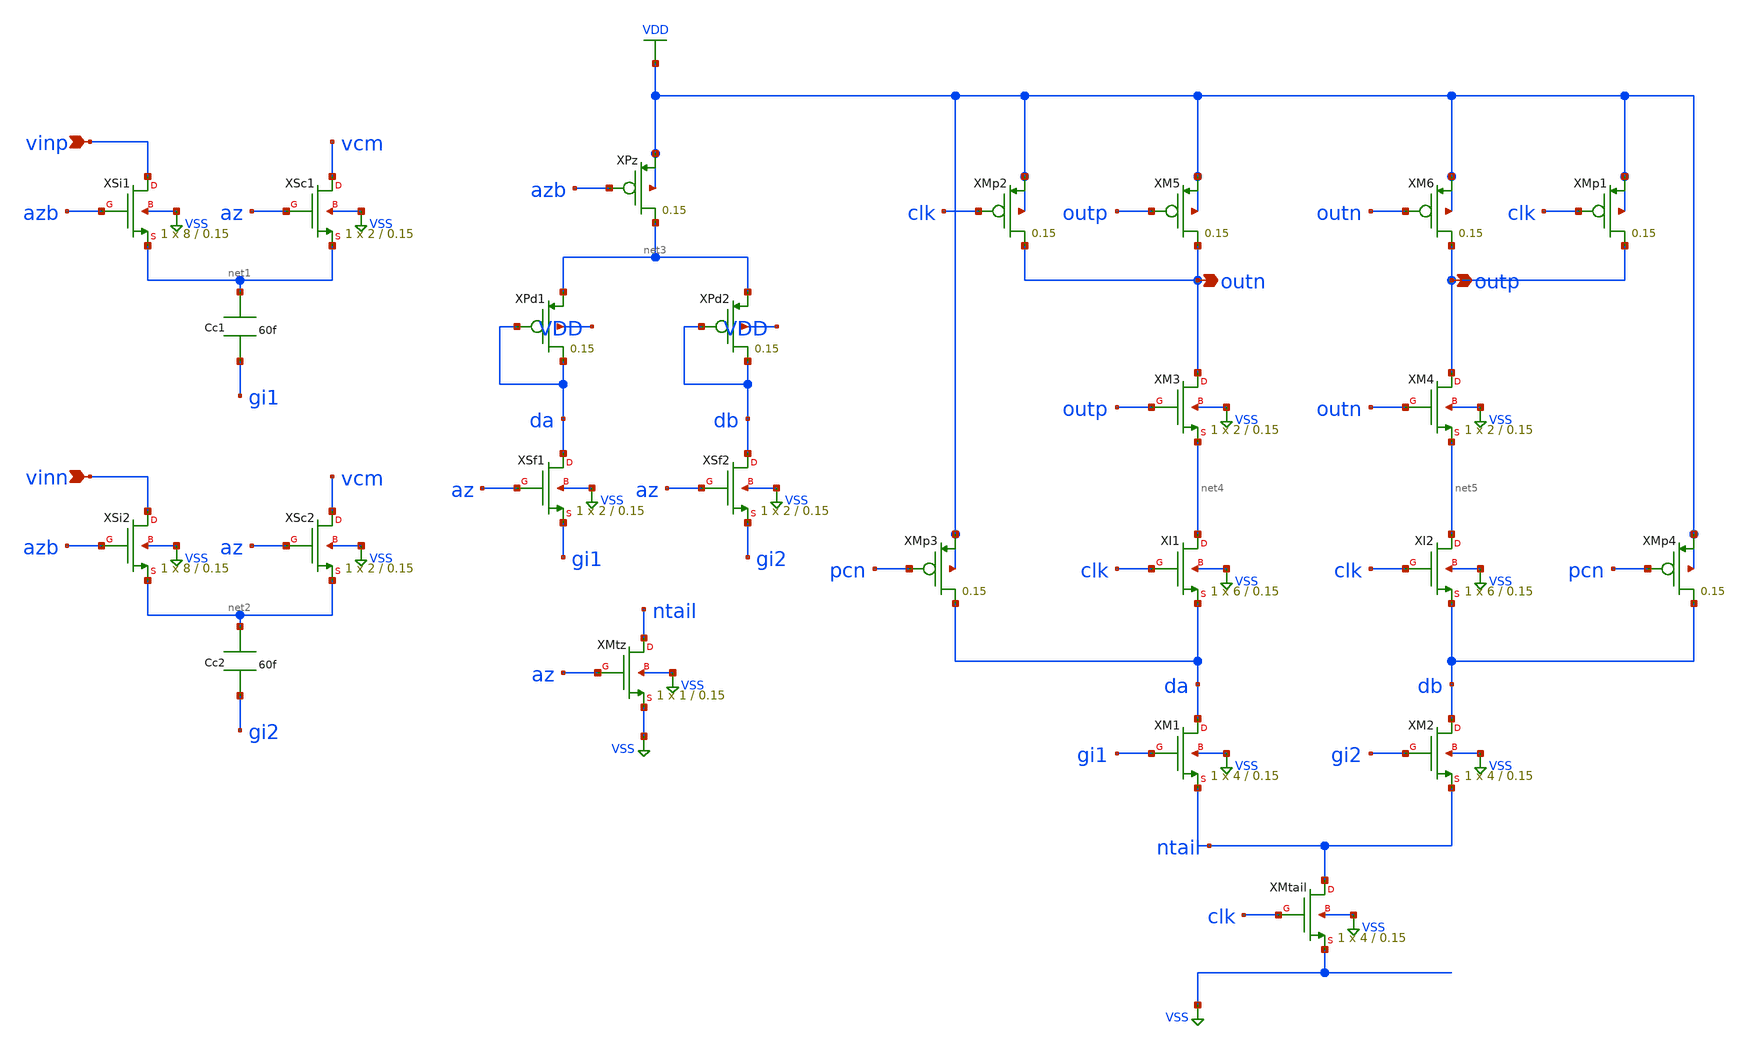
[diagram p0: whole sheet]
** sch_path: eda/hero/schematics/dong_autozero.sch
**.subckt dong_autozero vinp vinn outn outp
*.ipin vinp
*.ipin vinn
*.opin outn
*.opin outp
XXSi1 vinp azb net1 VSS sky130_fd_pr__sky130_fd_pr__nfet_01v8 L=0.15 W=8 nrd='0.29 / W' nrs='0.29 / W'
+ sa=0 sb=0 sd=0 mult=1 m=1
XXSc1 vcm az net1 VSS sky130_fd_pr__sky130_fd_pr__nfet_01v8 L=0.15 W=2 nrd='0.29 / W' nrs='0.29 / W'
+ sa=0 sb=0 sd=0 mult=1 m=1
XXSi2 vinn azb net2 VSS sky130_fd_pr__sky130_fd_pr__nfet_01v8 L=0.15 W=8 nrd='0.29 / W' nrs='0.29 / W'
+ sa=0 sb=0 sd=0 mult=1 m=1
XXSc2 vcm az net2 VSS sky130_fd_pr__sky130_fd_pr__nfet_01v8 L=0.15 W=2 nrd='0.29 / W' nrs='0.29 / W'
+ sa=0 sb=0 sd=0 mult=1 m=1
XXPz net3 azb VDD VDD sky130_fd_pr__sky130_fd_pr__pfet_01v8 L=0.15 W=4 nrd='0.29 / W' nrs='0.29 / W'
+ sa=0 sb=0 sd=0 mult=1 m=1
XXPd1 da da net3 VDD sky130_fd_pr__sky130_fd_pr__pfet_01v8 L=0.15 W=3 nrd='0.29 / W' nrs='0.29 / W' sa=0
+ sb=0 sd=0 mult=1 m=1
XXPd2 db db net3 VDD sky130_fd_pr__sky130_fd_pr__pfet_01v8 L=0.15 W=3 nrd='0.29 / W' nrs='0.29 / W' sa=0
+ sb=0 sd=0 mult=1 m=1
XXSf1 da az gi1 VSS sky130_fd_pr__sky130_fd_pr__nfet_01v8 L=0.15 W=2 nrd='0.29 / W' nrs='0.29 / W' sa=0
+ sb=0 sd=0 mult=1 m=1
XXSf2 db az gi2 VSS sky130_fd_pr__sky130_fd_pr__nfet_01v8 L=0.15 W=2 nrd='0.29 / W' nrs='0.29 / W' sa=0
+ sb=0 sd=0 mult=1 m=1
XXMtz ntail az VSS VSS sky130_fd_pr__sky130_fd_pr__nfet_01v8 L=0.15 W=1 nrd='0.29 / W' nrs='0.29 / W'
+ sa=0 sb=0 sd=0 mult=1 m=1
XXMp2 outn clk VDD VDD sky130_fd_pr__sky130_fd_pr__pfet_01v8 L=0.15 W=2 nrd='0.29 / W' nrs='0.29 / W'
+ sa=0 sb=0 sd=0 mult=1 m=1
XXM5 outn outp VDD VDD sky130_fd_pr__sky130_fd_pr__pfet_01v8 L=0.15 W=2 nrd='0.29 / W' nrs='0.29 / W'
+ sa=0 sb=0 sd=0 mult=1 m=1
XXM6 outp outn VDD VDD sky130_fd_pr__sky130_fd_pr__pfet_01v8 L=0.15 W=2 nrd='0.29 / W' nrs='0.29 / W'
+ sa=0 sb=0 sd=0 mult=1 m=1
XXMp1 outp clk VDD VDD sky130_fd_pr__sky130_fd_pr__pfet_01v8 L=0.15 W=2 nrd='0.29 / W' nrs='0.29 / W'
+ sa=0 sb=0 sd=0 mult=1 m=1
XXM3 outn outp net4 VSS sky130_fd_pr__sky130_fd_pr__nfet_01v8 L=0.15 W=2 nrd='0.29 / W' nrs='0.29 / W'
+ sa=0 sb=0 sd=0 mult=1 m=1
XXM4 outp outn net5 VSS sky130_fd_pr__sky130_fd_pr__nfet_01v8 L=0.15 W=2 nrd='0.29 / W' nrs='0.29 / W'
+ sa=0 sb=0 sd=0 mult=1 m=1
XXMp3 da pcn VDD VDD sky130_fd_pr__sky130_fd_pr__pfet_01v8 L=0.15 W=2 nrd='0.29 / W' nrs='0.29 / W' sa=0
+ sb=0 sd=0 mult=1 m=1
XXI1 net4 clk da VSS sky130_fd_pr__sky130_fd_pr__nfet_01v8 L=0.15 W=6 nrd='0.29 / W' nrs='0.29 / W' sa=0
+ sb=0 sd=0 mult=1 m=1
XXI2 net5 clk db VSS sky130_fd_pr__sky130_fd_pr__nfet_01v8 L=0.15 W=6 nrd='0.29 / W' nrs='0.29 / W' sa=0
+ sb=0 sd=0 mult=1 m=1
XXMp4 db pcn VDD VDD sky130_fd_pr__sky130_fd_pr__pfet_01v8 L=0.15 W=2 nrd='0.29 / W' nrs='0.29 / W' sa=0
+ sb=0 sd=0 mult=1 m=1
XXM1 da gi1 ntail VSS sky130_fd_pr__sky130_fd_pr__nfet_01v8 L=0.15 W=4 nrd='0.29 / W' nrs='0.29 / W'
+ sa=0 sb=0 sd=0 mult=1 m=1
XXM2 db gi2 ntail VSS sky130_fd_pr__sky130_fd_pr__nfet_01v8 L=0.15 W=4 nrd='0.29 / W' nrs='0.29 / W'
+ sa=0 sb=0 sd=0 mult=1 m=1
XXMtail ntail clk VSS VSS sky130_fd_pr__sky130_fd_pr__nfet_01v8 L=0.15 W=4 nrd='0.29 / W' nrs='0.29 / W'
+ sa=0 sb=0 sd=0 mult=1 m=1
Cc1 net1 gi1 60f m=1
Cc2 net2 gi2 60f m=1
**.ends
.GLOBAL VSS
.GLOBAL VDD
.end
